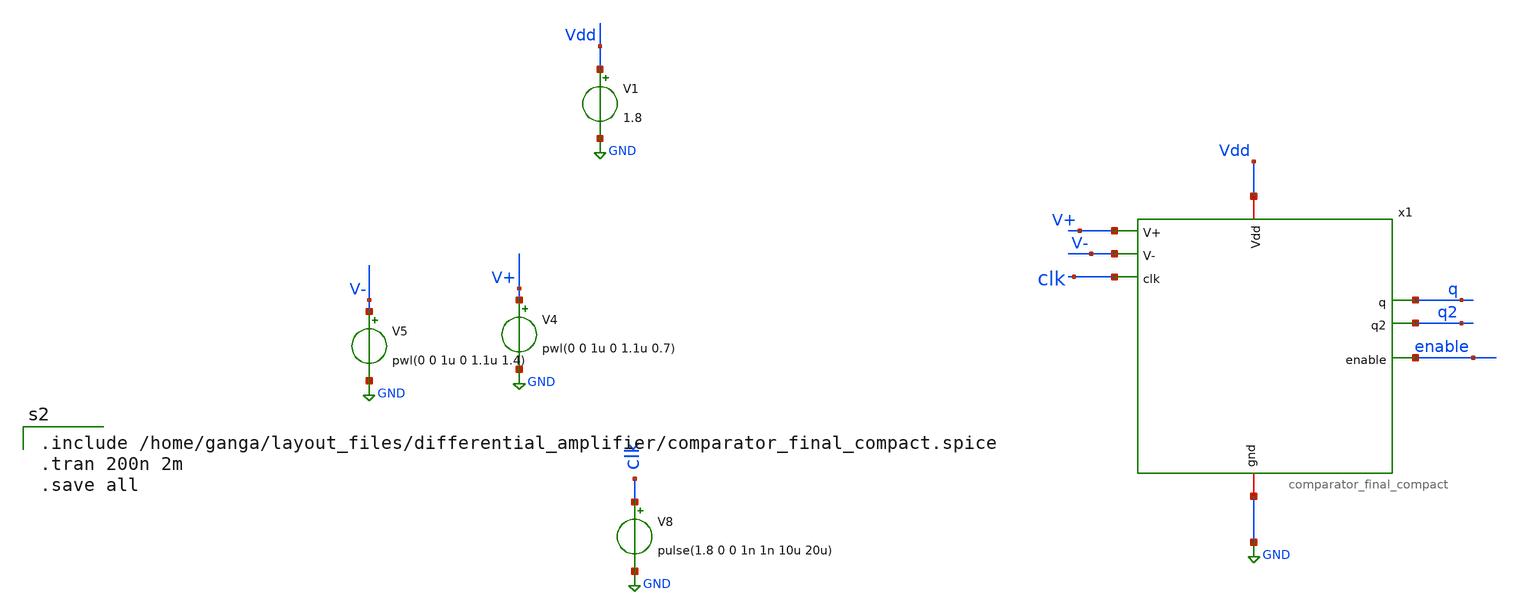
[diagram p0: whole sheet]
** sch_path: xschem/charge_pumps2/comparator_finaltest.sch
**.subckt comparator_finaltest
x1 Vdd GND V+ q enable clk V- q2 comparator_final_compact
V1 Vdd GND 1.8
V4 V+ GND pwl(0 0 1u 0 1.1u 0.7)
V5 V- GND pwl(0 0 1u 0 1.1u 1.4)
V8 clk GND pulse(1.8 0 0 1n 1n 10u 20u)
**** begin user architecture code

** opencircuitdesign pdks install
.lib $::SKYWATER_MODELS/sky130.lib.spice tt



.include /home/ganga/layout_files/differential_amplifier/comparator_final_compact.spice
.tran 200n 2m
.save all

**** end user architecture code
**.ends
.GLOBAL GND
.end
